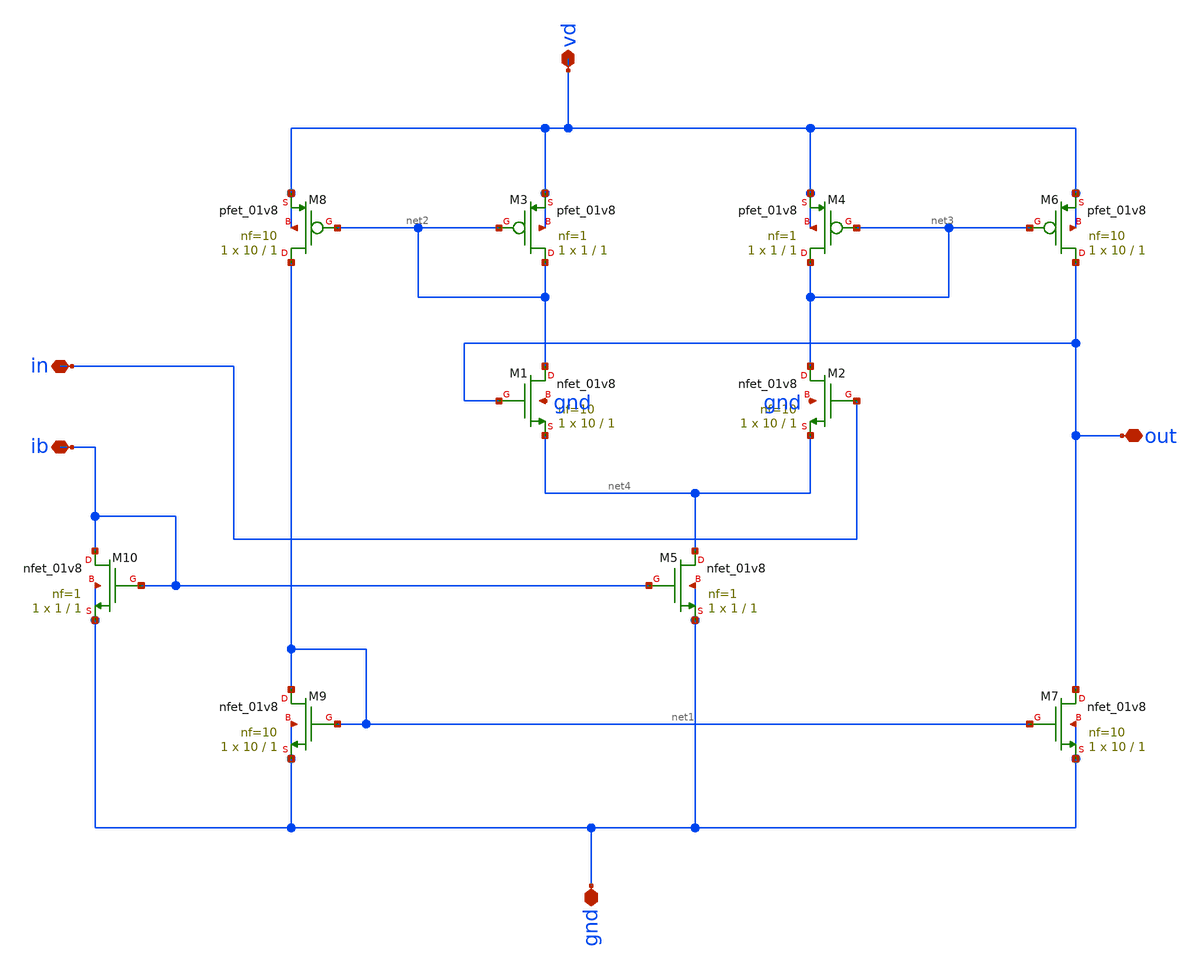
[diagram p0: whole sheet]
** sch_path: buffer/xschem/buffer.sch
* Copyright 2020 Stefan Frederik Schippers
* Licensed under the Apache License, Version 2.0 (the "License");
* you may not use this file except in compliance with the License.
* You may obtain a copy of the License at
* https://www.apache.org/licenses/LICENSE-2.0
* Unless required by applicable law or agreed to in writing, software
* distributed under the License is distributed on an "AS IS" BASIS,
* WITHOUT WARRANTIES OR CONDITIONS OF ANY KIND, either express or implied.
* See the License for the specific language governing permissions and
* limitations under the License.
**.subckt buffer vd ib out in gnd
*.iopin vd
*.iopin ib
*.iopin out
*.iopin in
*.iopin gnd
XM3 net2 net2 vd vd sky130_fd_pr__pfet_01v8 L=1 W=1 nf=1 ad='int((nf+1)/2) * W/nf * 0.29' as='int((nf+2)/2) * W/nf * 0.29'
+ pd='2*int((nf+1)/2) * (W/nf + 0.29)' ps='2*int((nf+2)/2) * (W/nf + 0.29)' nrd='0.29 / W' nrs='0.29 / W'
+ sa=0 sb=0 sd=0 mult=1 m=1
XM1 net2 out net4 gnd sky130_fd_pr__nfet_01v8 L=1 W=10 nf=10 ad='int((nf+1)/2) * W/nf * 0.29' as='int((nf+2)/2) * W/nf * 0.29'
+ pd='2*int((nf+1)/2) * (W/nf + 0.29)' ps='2*int((nf+2)/2) * (W/nf + 0.29)' nrd='0.29 / W' nrs='0.29 / W'
+ sa=0 sb=0 sd=0 mult=1 m=1
XM2 net3 in net4 gnd sky130_fd_pr__nfet_01v8 L=1 W=10 nf=10 ad='int((nf+1)/2) * W/nf * 0.29' as='int((nf+2)/2) * W/nf * 0.29'
+ pd='2*int((nf+1)/2) * (W/nf + 0.29)' ps='2*int((nf+2)/2) * (W/nf + 0.29)' nrd='0.29 / W' nrs='0.29 / W'
+ sa=0 sb=0 sd=0 mult=1 m=1
XM4 net3 net3 vd vd sky130_fd_pr__pfet_01v8 L=1 W=1 nf=1 ad='int((nf+1)/2) * W/nf * 0.29' as='int((nf+2)/2) * W/nf * 0.29'
+ pd='2*int((nf+1)/2) * (W/nf + 0.29)' ps='2*int((nf+2)/2) * (W/nf + 0.29)' nrd='0.29 / W' nrs='0.29 / W'
+ sa=0 sb=0 sd=0 mult=1 m=1
XM5 net4 ib gnd gnd sky130_fd_pr__nfet_01v8 L=1 W=1 nf=1 ad='int((nf+1)/2) * W/nf * 0.29' as='int((nf+2)/2) * W/nf * 0.29'
+ pd='2*int((nf+1)/2) * (W/nf + 0.29)' ps='2*int((nf+2)/2) * (W/nf + 0.29)' nrd='0.29 / W' nrs='0.29 / W'
+ sa=0 sb=0 sd=0 mult=1 m=1
XM6 out net3 vd vd sky130_fd_pr__pfet_01v8 L=1 W=10 nf=10 ad='int((nf+1)/2) * W/nf * 0.29' as='int((nf+2)/2) * W/nf * 0.29'
+ pd='2*int((nf+1)/2) * (W/nf + 0.29)' ps='2*int((nf+2)/2) * (W/nf + 0.29)' nrd='0.29 / W' nrs='0.29 / W'
+ sa=0 sb=0 sd=0 mult=1 m=1
XM7 out net1 gnd gnd sky130_fd_pr__nfet_01v8 L=1 W=10 nf=10 ad='int((nf+1)/2) * W/nf * 0.29' as='int((nf+2)/2) * W/nf * 0.29'
+ pd='2*int((nf+1)/2) * (W/nf + 0.29)' ps='2*int((nf+2)/2) * (W/nf + 0.29)' nrd='0.29 / W' nrs='0.29 / W'
+ sa=0 sb=0 sd=0 mult=1 m=1
XM8 net1 net2 vd vd sky130_fd_pr__pfet_01v8 L=1 W=10 nf=10 ad='int((nf+1)/2) * W/nf * 0.29' as='int((nf+2)/2) * W/nf * 0.29'
+ pd='2*int((nf+1)/2) * (W/nf + 0.29)' ps='2*int((nf+2)/2) * (W/nf + 0.29)' nrd='0.29 / W' nrs='0.29 / W'
+ sa=0 sb=0 sd=0 mult=1 m=1
XM9 net1 net1 gnd gnd sky130_fd_pr__nfet_01v8 L=1 W=10 nf=10 ad='int((nf+1)/2) * W/nf * 0.29' as='int((nf+2)/2) * W/nf * 0.29'
+ pd='2*int((nf+1)/2) * (W/nf + 0.29)' ps='2*int((nf+2)/2) * (W/nf + 0.29)' nrd='0.29 / W' nrs='0.29 / W'
+ sa=0 sb=0 sd=0 mult=1 m=1
XM10 ib ib gnd gnd sky130_fd_pr__nfet_01v8 L=1 W=1 nf=1 ad='int((nf+1)/2) * W/nf * 0.29' as='int((nf+2)/2) * W/nf * 0.29'
+ pd='2*int((nf+1)/2) * (W/nf + 0.29)' ps='2*int((nf+2)/2) * (W/nf + 0.29)' nrd='0.29 / W' nrs='0.29 / W'
+ sa=0 sb=0 sd=0 mult=1 m=1
**.ends
.end
